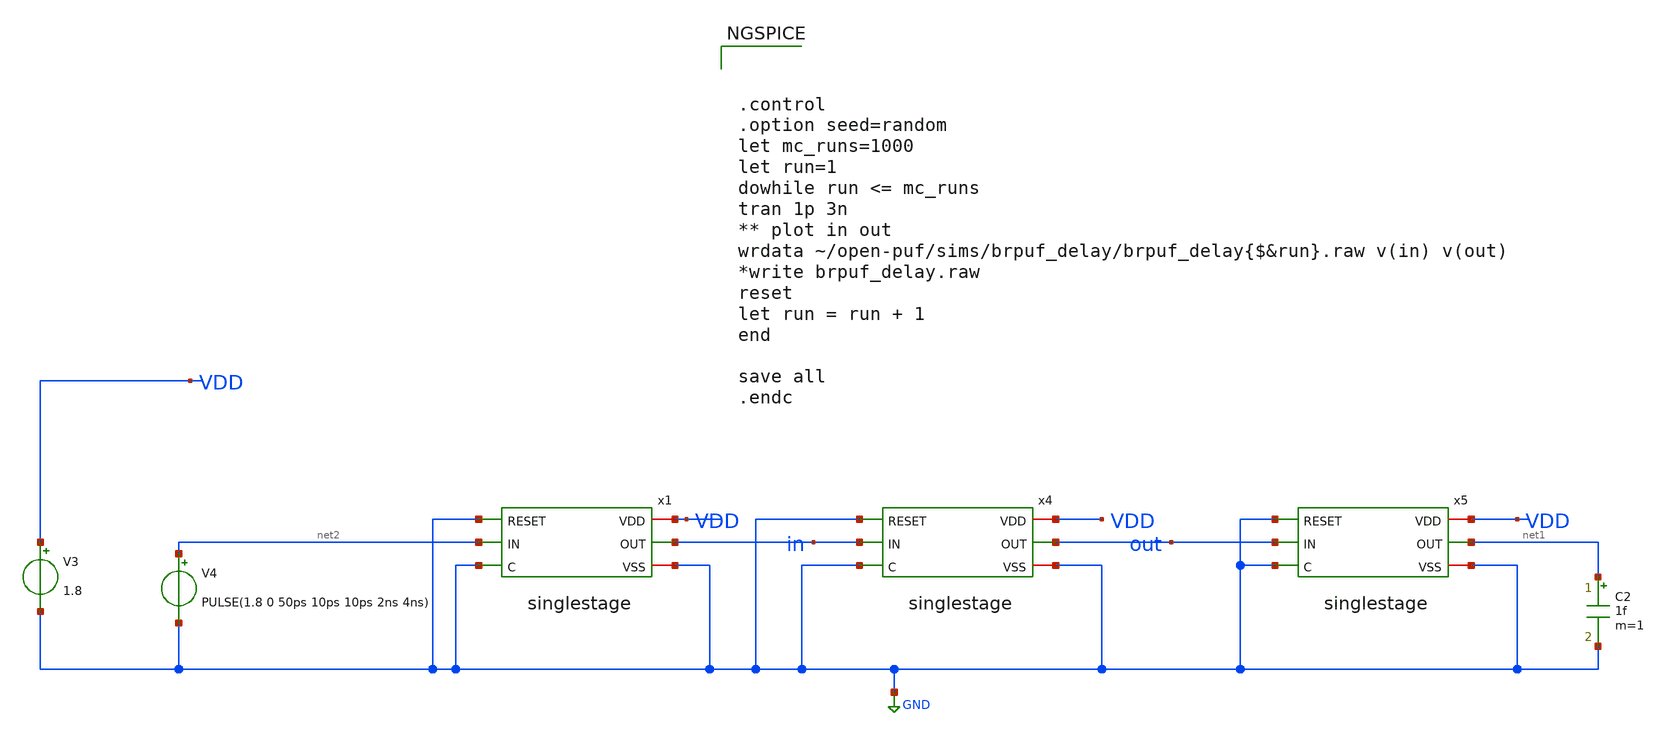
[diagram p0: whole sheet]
** sch_path: design/brpuf_delay.sch
**.subckt brpuf_delay
V3 VDD GND 1.8
V4 net2 GND PULSE(1.8 0 50ps 10ps 10ps 2ns 4ns)
C2 net1 GND 1f m=1
x4 GND VDD GND out in GND singlestage
x5 GND VDD GND net1 out GND singlestage
x1 GND VDD GND in net2 GND singlestage
**** begin user architecture code

** opencircuitdesign pdks install
.lib $::SKYWATER_MODELS/sky130.lib.spice tt_mm
.include $::SKYWATER_STDCELLS/sky130_fd_sc_hd.spice





.control
.option seed=random
let mc_runs=1000
let run=1
dowhile run <= mc_runs
tran 1p 3n
** plot in out
wrdata ~/open-puf/sims/brpuf_delay/brpuf_delay{$&run}.raw v(in) v(out)
*write brpuf_delay.raw
reset
let run = run + 1
end

save all
.endc


**** end user architecture code
**.ends

* expanding   symbol:  design/singlestage.sym # of pins=6
** sym_path: design/singlestage.sym
** sch_path: design/singlestage.sch
.subckt singlestage RESET VDD VSS OUT IN C
*.ipin IN
*.ipin C
*.ipin RESET
*.iopin VSS
*.iopin VDD
*.opin OUT
x1 RESET net1 VSS VSS VDD VDD net3 sky130_fd_sc_hd__nor2_1
x2 RESET net2 VSS VSS VDD VDD net4 sky130_fd_sc_hd__nor2_1
x3 net6 VSS net1 VDD IN net5 net2 demux2-1
x4 net6 VSS net3 VDD OUT net5 net4 mux2-1
x5 net5 VSS VSS VDD VDD net6 sky130_fd_sc_hd__inv_1
XM1 net1 net6 VDD VDD sky130_fd_pr__pfet_01v8_hvt L=0.15 W=1 nf=1 ad='int((nf+1)/2) * W/nf * 0.29' as='int((nf+2)/2) * W/nf * 0.29'
+ pd='2*int((nf+1)/2) * (W/nf + 0.29)' ps='2*int((nf+2)/2) * (W/nf + 0.29)' nrd='0.29 / W' nrs='0.29 / W'
+ sa=0 sb=0 sd=0 mult=1 m=1
XM2 net2 net5 VDD VDD sky130_fd_pr__pfet_01v8_hvt L=0.15 W=1 nf=1 ad='int((nf+1)/2) * W/nf * 0.29' as='int((nf+2)/2) * W/nf * 0.29'
+ pd='2*int((nf+1)/2) * (W/nf + 0.29)' ps='2*int((nf+2)/2) * (W/nf + 0.29)' nrd='0.29 / W' nrs='0.29 / W'
+ sa=0 sb=0 sd=0 mult=1 m=1
x6 C VSS VSS VDD VDD net5 sky130_fd_sc_hd__inv_1
.ends


* expanding   symbol:  demux2-1.sym # of pins=7
** sym_path: xiaolin/demux2-1.sym
** sch_path: xiaolin/demux2-1.sch
.subckt demux2-1 S VSS OUT1 VDD IN Sbar OUT2
*.ipin Sbar
*.ipin S
*.iopin VSS
*.iopin VDD
*.opin OUT1
*.opin OUT2
*.ipin IN
XM2 IN S OUT1 VSS sky130_fd_pr__nfet_01v8 L=0.15 W=0.65 nf=1 ad='int((nf+1)/2) * W/nf * 0.29' as='int((nf+2)/2) * W/nf * 0.29'
+ pd='2*int((nf+1)/2) * (W/nf + 0.29)' ps='2*int((nf+2)/2) * (W/nf + 0.29)' nrd='0.29 / W' nrs='0.29 / W'
+ sa=0 sb=0 sd=0 mult=1 m=1
XM1 IN Sbar OUT2 VSS sky130_fd_pr__nfet_01v8 L=0.15 W=0.65 nf=1 ad='int((nf+1)/2) * W/nf * 0.29' as='int((nf+2)/2) * W/nf * 0.29'
+ pd='2*int((nf+1)/2) * (W/nf + 0.29)' ps='2*int((nf+2)/2) * (W/nf + 0.29)' nrd='0.29 / W' nrs='0.29 / W'
+ sa=0 sb=0 sd=0 mult=1 m=1
XM3 IN S OUT2 VDD sky130_fd_pr__pfet_01v8_hvt L=0.15 W=1 nf=1 ad='int((nf+1)/2) * W/nf * 0.29' as='int((nf+2)/2) * W/nf * 0.29'
+ pd='2*int((nf+1)/2) * (W/nf + 0.29)' ps='2*int((nf+2)/2) * (W/nf + 0.29)' nrd='0.29 / W' nrs='0.29 / W'
+ sa=0 sb=0 sd=0 mult=1 m=1
XM4 IN Sbar OUT1 VDD sky130_fd_pr__pfet_01v8_hvt L=0.15 W=1 nf=1 ad='int((nf+1)/2) * W/nf * 0.29' as='int((nf+2)/2) * W/nf * 0.29'
+ pd='2*int((nf+1)/2) * (W/nf + 0.29)' ps='2*int((nf+2)/2) * (W/nf + 0.29)' nrd='0.29 / W' nrs='0.29 / W'
+ sa=0 sb=0 sd=0 mult=1 m=1
XM5 IN S OUT2 VDD sky130_fd_pr__pfet_01v8_hvt L=0.15 W=1 nf=1 ad='int((nf+1)/2) * W/nf * 0.29' as='int((nf+2)/2) * W/nf * 0.29'
+ pd='2*int((nf+1)/2) * (W/nf + 0.29)' ps='2*int((nf+2)/2) * (W/nf + 0.29)' nrd='0.29 / W' nrs='0.29 / W'
+ sa=0 sb=0 sd=0 mult=1 m=1
.ends


* expanding   symbol:  mux2-1.sym # of pins=7
** sym_path: design/mux2-1.sym
** sch_path: design/mux2-1.sch
.subckt mux2-1 S VSS IN1 VDD OUT Sbar IN2
*.ipin IN1
*.ipin IN2
*.ipin Sbar
*.ipin S
*.opin OUT
*.iopin VSS
*.iopin VDD
XM2 IN1 S OUT VSS sky130_fd_pr__nfet_01v8 L=0.15 W=0.65 nf=1 ad='int((nf+1)/2) * W/nf * 0.29' as='int((nf+2)/2) * W/nf * 0.29'
+ pd='2*int((nf+1)/2) * (W/nf + 0.29)' ps='2*int((nf+2)/2) * (W/nf + 0.29)' nrd='0.29 / W' nrs='0.29 / W'
+ sa=0 sb=0 sd=0 mult=1 m=1
XM1 IN2 Sbar OUT VSS sky130_fd_pr__nfet_01v8 L=0.15 W=0.65 nf=1 ad='int((nf+1)/2) * W/nf * 0.29' as='int((nf+2)/2) * W/nf * 0.29'
+ pd='2*int((nf+1)/2) * (W/nf + 0.29)' ps='2*int((nf+2)/2) * (W/nf + 0.29)' nrd='0.29 / W' nrs='0.29 / W'
+ sa=0 sb=0 sd=0 mult=1 m=1
XM4 IN1 Sbar OUT VDD sky130_fd_pr__pfet_01v8_hvt L=0.15 W=1 nf=1 ad='int((nf+1)/2) * W/nf * 0.29' as='int((nf+2)/2) * W/nf * 0.29'
+ pd='2*int((nf+1)/2) * (W/nf + 0.29)' ps='2*int((nf+2)/2) * (W/nf + 0.29)' nrd='0.29 / W' nrs='0.29 / W'
+ sa=0 sb=0 sd=0 mult=1 m=1
XM5 IN2 S OUT VDD sky130_fd_pr__pfet_01v8_hvt L=0.15 W=1 nf=1 ad='int((nf+1)/2) * W/nf * 0.29' as='int((nf+2)/2) * W/nf * 0.29'
+ pd='2*int((nf+1)/2) * (W/nf + 0.29)' ps='2*int((nf+2)/2) * (W/nf + 0.29)' nrd='0.29 / W' nrs='0.29 / W'
+ sa=0 sb=0 sd=0 mult=1 m=1
.ends

.GLOBAL GND
.end
